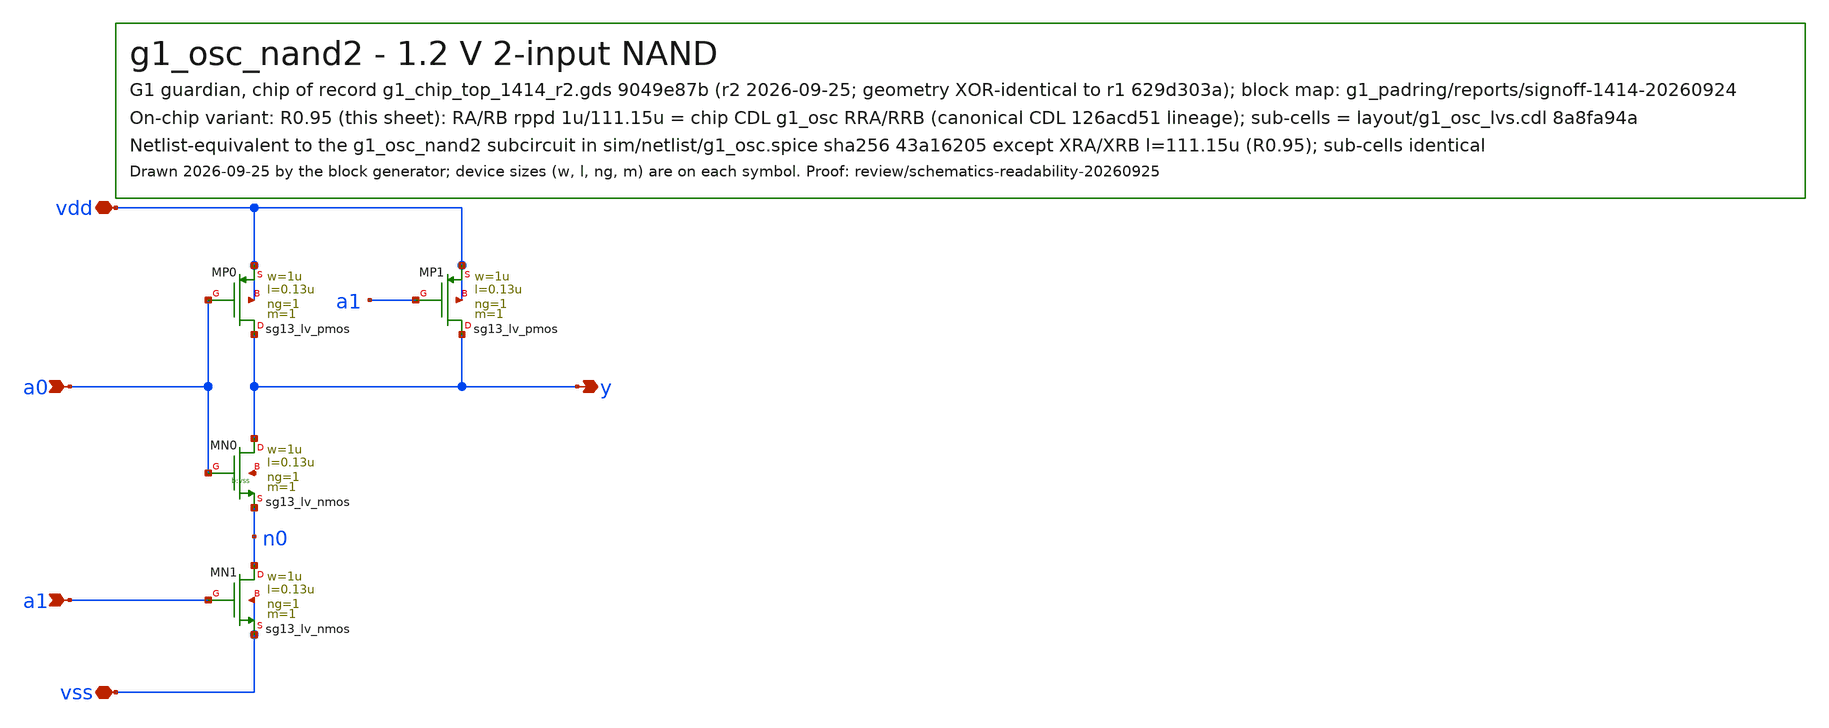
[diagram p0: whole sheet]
** sch_path: designs/g1-guardian/blocks/g1_osc/schematic/g1_osc_nand2.sch
**.subckt g1_osc_nand2 a0 a1 y vdd vss
*.ipin a0
*.ipin a1
*.opin y
*.iopin vdd
*.iopin vss
XMP0 y a0 vdd vdd sg13_lv_pmos w=1u l=0.13u ng=1 m=1 mm_ok=1
XMP1 y a1 vdd vdd sg13_lv_pmos w=1u l=0.13u ng=1 m=1 mm_ok=1
XMN0 y a0 n0 vss sg13_lv_nmos w=1u l=0.13u ng=1 m=1 mm_ok=1
XMN1 n0 a1 vss vss sg13_lv_nmos w=1u l=0.13u ng=1 m=1 mm_ok=1
**.ends
.end
